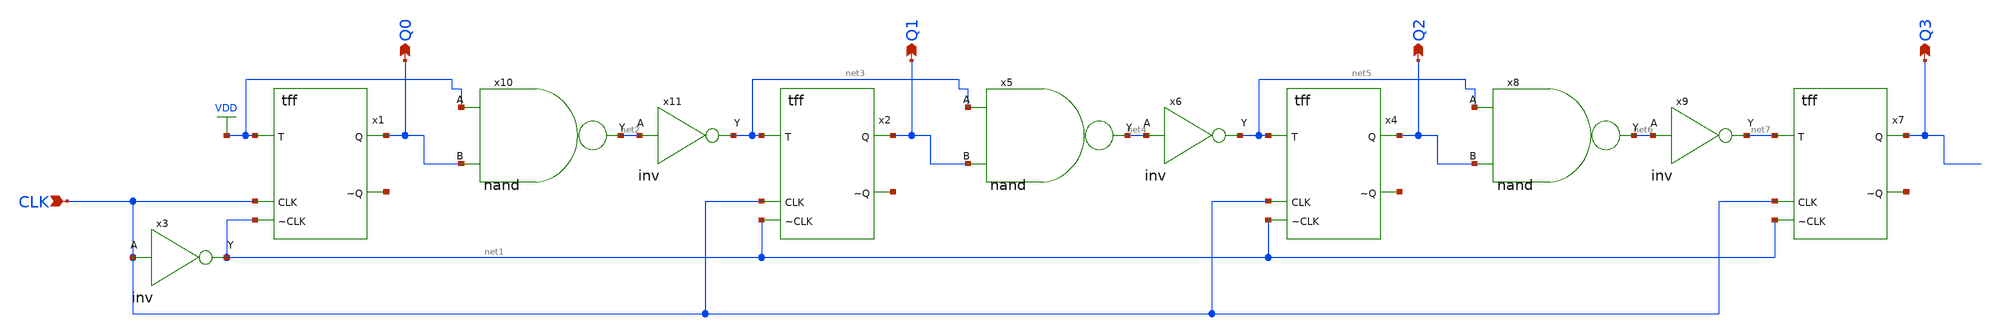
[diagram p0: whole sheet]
** sch_path: circuits/xschem/counter_4.sch
**.subckt counter_4 CLK Q0 Q1 Q2 Q3
*.ipin CLK
*.opin Q0
*.opin Q1
*.opin Q2
*.opin Q3
x1 VDD Q0 CLK net1 net8 tff
x2 net3 Q1 CLK net1 net9 tff
x3 net1 CLK inv
x10 VDD net2 Q0 nand
x11 net3 net2 inv
x4 net5 Q2 CLK net1 net10 tff
x5 net3 net4 Q1 nand
x6 net5 net4 inv
x7 net7 Q3 CLK net1 net11 tff
x8 net5 net6 Q2 nand
x9 net7 net6 inv
**.ends
.GLOBAL VDD
.end
